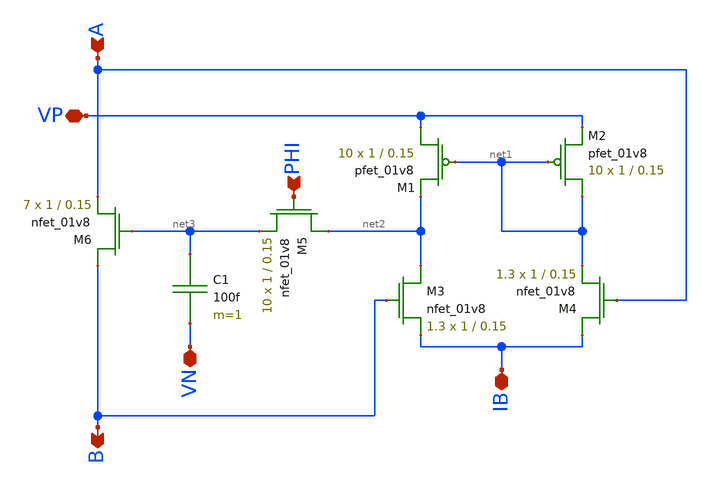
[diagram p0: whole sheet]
** sch_path: schematic/mem_sax.sch
**.subckt mem_sax A B PHI VP IB VN
*.ipin A
*.opin B
*.ipin PHI
*.iopin VP
*.iopin IB
*.iopin VN
XM1 VP net1 net2 VDD sky130_fd_pr__pfet_01v8 L=0.15 W=1 nf=1 ad='int((nf+1)/2) * W/nf * 0.29' as='int((nf+2)/2) * W/nf * 0.29'
+ pd='2*int((nf+1)/2) * (W/nf + 0.29)' ps='2*int((nf+2)/2) * (W/nf + 0.29)' nrd='0.29 / W' nrs='0.29 / W'
+ sa=0 sb=0 sd=0 mult=10 m=10
XM2 net1 net1 VP VDD sky130_fd_pr__pfet_01v8 L=0.15 W=1 nf=1 ad='int((nf+1)/2) * W/nf * 0.29' as='int((nf+2)/2) * W/nf * 0.29'
+ pd='2*int((nf+1)/2) * (W/nf + 0.29)' ps='2*int((nf+2)/2) * (W/nf + 0.29)' nrd='0.29 / W' nrs='0.29 / W'
+ sa=0 sb=0 sd=0 mult=10 m=10
XM3 net2 B IB GND sky130_fd_pr__nfet_01v8 L=0.15 W=1 nf=1 ad='int((nf+1)/2) * W/nf * 0.29' as='int((nf+2)/2) * W/nf * 0.29'
+ pd='2*int((nf+1)/2) * (W/nf + 0.29)' ps='2*int((nf+2)/2) * (W/nf + 0.29)' nrd='0.29 / W' nrs='0.29 / W'
+ sa=0 sb=0 sd=0 mult=1.3 m=1.3
XM4 IB A net1 GND sky130_fd_pr__nfet_01v8 L=0.15 W=1 nf=1 ad='int((nf+1)/2) * W/nf * 0.29' as='int((nf+2)/2) * W/nf * 0.29'
+ pd='2*int((nf+1)/2) * (W/nf + 0.29)' ps='2*int((nf+2)/2) * (W/nf + 0.29)' nrd='0.29 / W' nrs='0.29 / W'
+ sa=0 sb=0 sd=0 mult=1.3 m=1.3
XM5 net2 PHI net3 GND sky130_fd_pr__nfet_01v8 L=0.15 W=1 nf=1 ad='int((nf+1)/2) * W/nf * 0.29' as='int((nf+2)/2) * W/nf * 0.29'
+ pd='2*int((nf+1)/2) * (W/nf + 0.29)' ps='2*int((nf+2)/2) * (W/nf + 0.29)' nrd='0.29 / W' nrs='0.29 / W'
+ sa=0 sb=0 sd=0 mult=10 m=10
XM6 B net3 A GND sky130_fd_pr__nfet_01v8 L=0.15 W=1 nf=1 ad='int((nf+1)/2) * W/nf * 0.29' as='int((nf+2)/2) * W/nf * 0.29'
+ pd='2*int((nf+1)/2) * (W/nf + 0.29)' ps='2*int((nf+2)/2) * (W/nf + 0.29)' nrd='0.29 / W' nrs='0.29 / W'
+ sa=0 sb=0 sd=0 mult=7 m=7
C1 net3 VN 100f m=1
**.ends
.end
